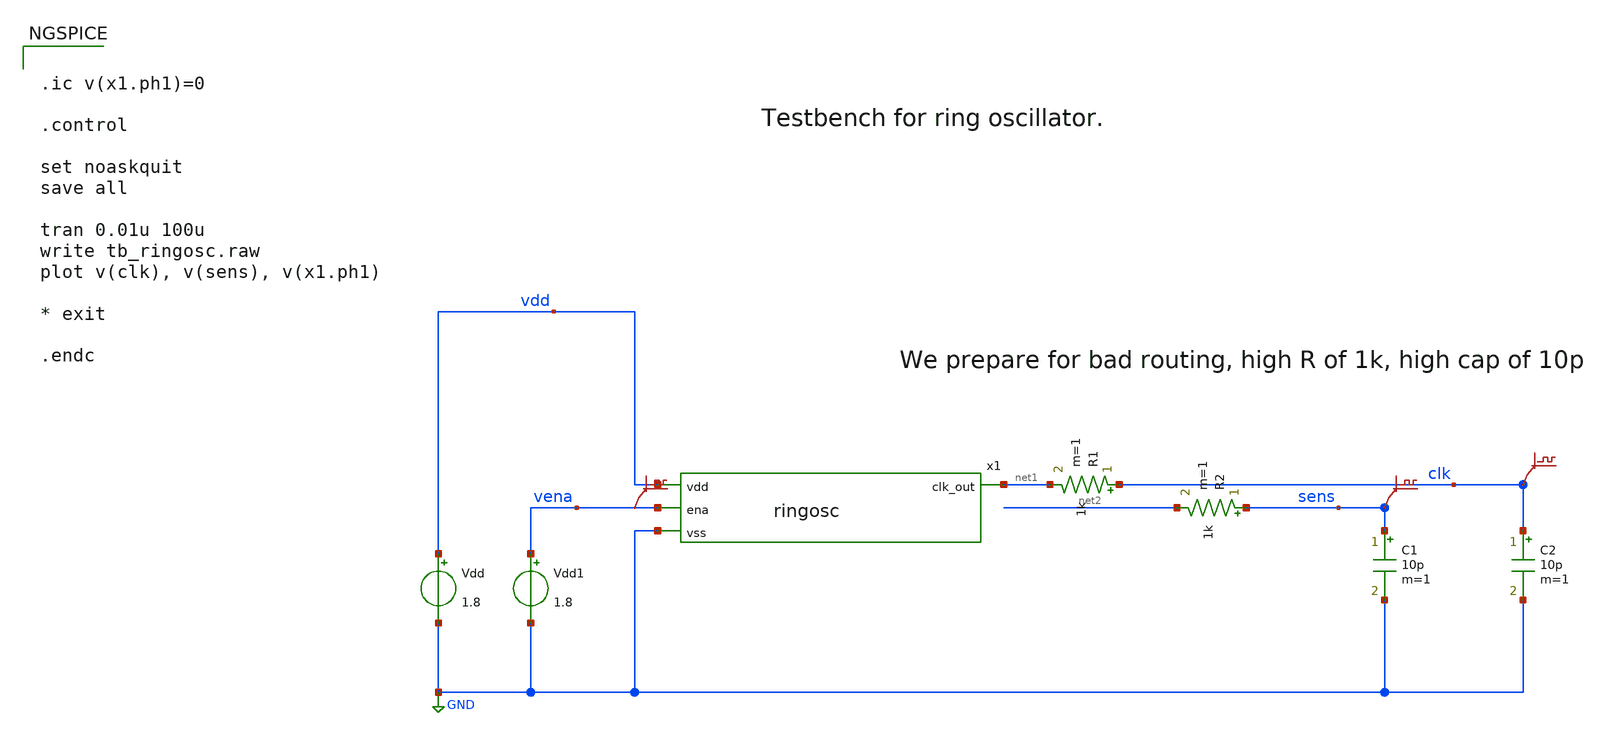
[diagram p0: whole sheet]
** sch_path: xschem/tb_ringosc.sch
**.subckt tb_ringosc
Vdd vdd GND 1.8
x1 vdd net1 vena GND ringosc
C1 sens GND 10p m=1
C2 clk GND 10p m=1
.save v(clk)
.save v(sens)
R1 clk net1 1k m=1
R2 sens net2 1k m=1
.save v(vena)
Vdd1 vena GND 1.8
**** begin user architecture code
 ** manual skywater pdks install (with patches applied)
* .lib $::SKYWATER_MODELS/models/sky130.lib.spice tt

** opencircuitdesign pdks install
.lib $::SKYWATER_MODELS/sky130.lib.spice.tt.red tt

.param mc_mm_switch=0
.param mc_pr_switch=0



.ic v(x1.ph1)=0

.control

set noaskquit
save all

tran 0.01u 100u
write tb_ringosc.raw
plot v(clk), v(sens), v(x1.ph1)

* exit

.endc


**** end user architecture code
**.ends

* expanding   symbol:  ringosc.sym # of pins=4
** sym_path: ringosc.sym
** sch_path: ringosc.sch
.subckt ringosc vdd clk_out ena vss
*.ipin vdd
*.ipin vss
*.opin clk_out
*.ipin ena
.save v(ph1)
.save v(ph2)
.save v(ph3)
x1 net1 net2 net3 net4 ringosc_delay
x2 net5 net6 net7 net8 ringosc_delay
x3 net9 net10 net11 net12 ringosc_delay
x4 vdd ph1 net13 vss ringosc_buf
x5 vdd ph2 net14 vss ringosc_buf
x6 vdd ph3 clk_out vss ringosc_buf
* noconn #net13
* noconn #net14
.save v(ena)
.ends


* expanding   symbol:  ringosc_delay.sym # of pins=4
** sym_path: xschem/ringosc_delay.sym
** sch_path: xschem/ringosc_delay.sch
.subckt ringosc_delay vdd in out vss
*.ipin vdd
*.ipin vss
*.ipin in
*.opin out
XM1 out in vdd vdd sky130_fd_pr__pfet_01v8 L=10 W=0.5 nf=1 ad='int((nf+1)/2) * W/nf * 0.29' as='int((nf+2)/2) * W/nf * 0.29'
+ pd='2*int((nf+1)/2) * (W/nf + 0.29)' ps='2*int((nf+2)/2) * (W/nf + 0.29)' nrd='0.29 / W' nrs='0.29 / W'
+ sa=0 sb=0 sd=0 mult=1 m=1
XM2 out in net1 vss sky130_fd_pr__nfet_01v8 L=10 W=0.5 nf=1 ad='int((nf+1)/2) * W/nf * 0.29' as='int((nf+2)/2) * W/nf * 0.29'
+ pd='2*int((nf+1)/2) * (W/nf + 0.29)' ps='2*int((nf+2)/2) * (W/nf + 0.29)' nrd='0.29 / W' nrs='0.29 / W'
+ sa=0 sb=0 sd=0 mult=1 m=1
XM4 vss out vss vss sky130_fd_pr__nfet_01v8 L=2 W=10 nf=1 ad='int((nf+1)/2) * W/nf * 0.29' as='int((nf+2)/2) * W/nf * 0.29'
+ pd='2*int((nf+1)/2) * (W/nf + 0.29)' ps='2*int((nf+2)/2) * (W/nf + 0.29)' nrd='0.29 / W' nrs='0.29 / W'
+ sa=0 sb=0 sd=0 mult=1 m=1
XM5 vdd out vdd vdd sky130_fd_pr__pfet_01v8 L=2 W=10 nf=1 ad='int((nf+1)/2) * W/nf * 0.29' as='int((nf+2)/2) * W/nf * 0.29'
+ pd='2*int((nf+1)/2) * (W/nf + 0.29)' ps='2*int((nf+2)/2) * (W/nf + 0.29)' nrd='0.29 / W' nrs='0.29 / W'
+ sa=0 sb=0 sd=0 mult=1 m=1
XM3 net1 in vss vss sky130_fd_pr__nfet_01v8 L=10 W=0.5 nf=1 ad='int((nf+1)/2) * W/nf * 0.29' as='int((nf+2)/2) * W/nf * 0.29'
+ pd='2*int((nf+1)/2) * (W/nf + 0.29)' ps='2*int((nf+2)/2) * (W/nf + 0.29)' nrd='0.29 / W' nrs='0.29 / W'
+ sa=0 sb=0 sd=0 mult=1 m=1
.ends


* expanding   symbol:  ringosc_buf.sym # of pins=4
** sym_path: xschem/ringosc_buf.sym
** sch_path: xschem/ringosc_buf.sch
.subckt ringosc_buf vdd in out vss
*.ipin vdd
*.ipin vss
*.ipin in
*.opin out
XM2 out in vss vss sky130_fd_pr__nfet_01v8 L=0.5 W=10 nf=1 ad='int((nf+1)/2) * W/nf * 0.29' as='int((nf+2)/2) * W/nf * 0.29'
+ pd='2*int((nf+1)/2) * (W/nf + 0.29)' ps='2*int((nf+2)/2) * (W/nf + 0.29)' nrd='0.29 / W' nrs='0.29 / W'
+ sa=0 sb=0 sd=0 mult=1 m=1
XM8 out in vdd vdd sky130_fd_pr__pfet_01v8 L=0.5 W=10 nf=1 ad='int((nf+1)/2) * W/nf * 0.29' as='int((nf+2)/2) * W/nf * 0.29'
+ pd='2*int((nf+1)/2) * (W/nf + 0.29)' ps='2*int((nf+2)/2) * (W/nf + 0.29)' nrd='0.29 / W' nrs='0.29 / W'
+ sa=0 sb=0 sd=0 mult=1 m=1
XM1 out in vdd vdd sky130_fd_pr__pfet_01v8 L=0.5 W=10 nf=1 ad='int((nf+1)/2) * W/nf * 0.29' as='int((nf+2)/2) * W/nf * 0.29'
+ pd='2*int((nf+1)/2) * (W/nf + 0.29)' ps='2*int((nf+2)/2) * (W/nf + 0.29)' nrd='0.29 / W' nrs='0.29 / W'
+ sa=0 sb=0 sd=0 mult=1 m=1
.ends

.GLOBAL GND
.end
